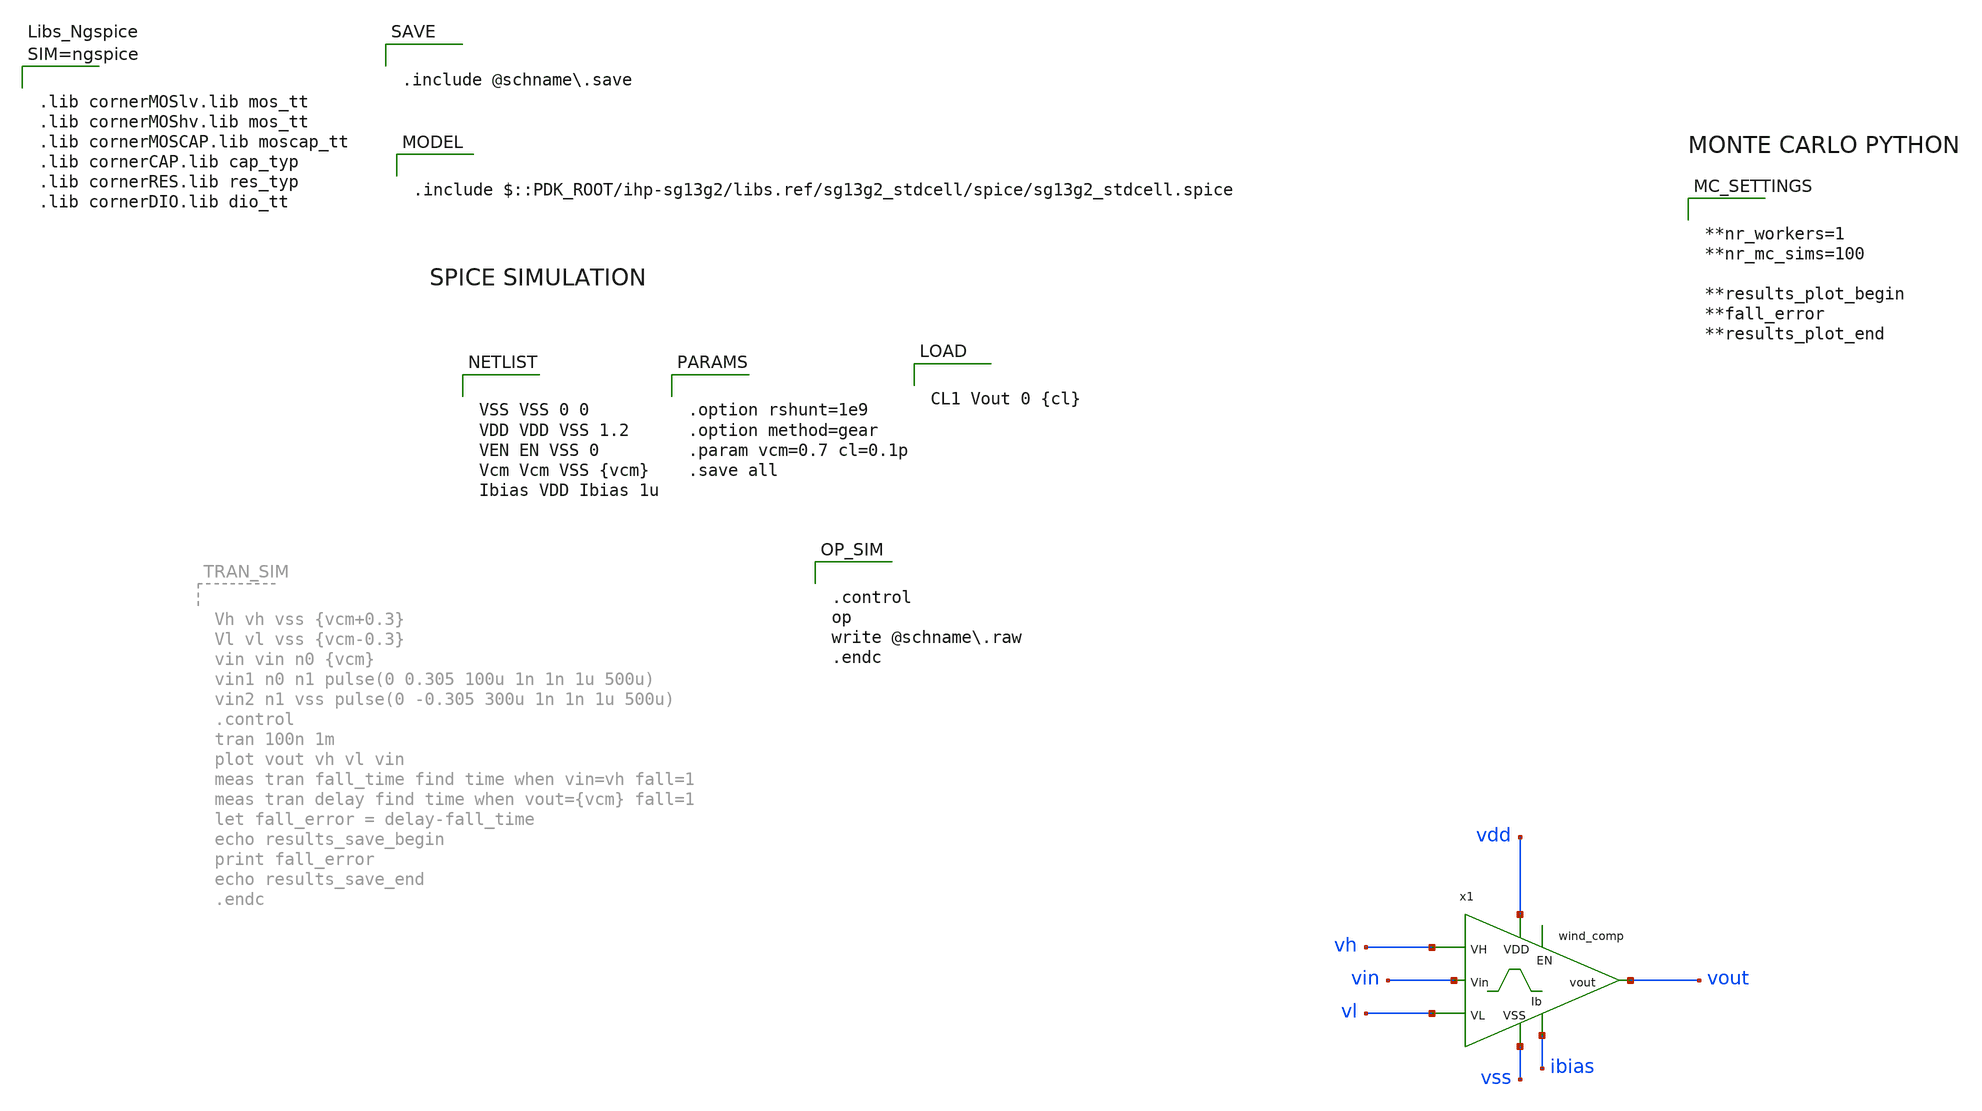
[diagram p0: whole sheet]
** sch_path: schematic/xschem/wind_comp/wind_comp_tb.sch

.include $::PDK_ROOT/ihp-sg13g2/libs.ref/sg13g2_stdcell/spice/sg13g2_stdcell.spice


**.subckt wind_comp_tb
x1 vdd vh vout vin vl ibias vss wind_comp
**** begin user architecture code


VSS VSS 0 0
VDD VDD VSS 1.2
VEN EN VSS 0
Vcm Vcm VSS {vcm}
Ibias VDD Ibias 1u



.control
op
write @schname.raw
.endc




.lib cornerMOSlv.lib mos_tt
.lib cornerMOShv.lib mos_tt
.lib cornerMOSCAP.lib moscap_tt
.lib cornerCAP.lib cap_typ
.lib cornerRES.lib res_typ
.lib cornerDIO.lib dio_tt





.option rshunt=1e9
.option method=gear
.param vcm=0.7 cl=0.1p
.save all




CL1 Vout 0 {cl}



.include @schname.save



**nr_workers=1
**nr_mc_sims=100

**results_plot_begin
**fall_error
**results_plot_end




Vh vh vss {vcm+0.3}
Vl vl vss {vcm-0.3}
vin vin vss sin({vcm} 0.4 1000)
.control
tran 100n 1m
plot vout vh vl vin
meas tran fall_time find time when vin=vh fall=1
meas tran delay find time when vout={vcm} fall=1
let fall_error = delay-fall_time
echo results_save_begin
print fall_error
echo results_save_end
.endc


**** end user architecture code
**.ends
.end
